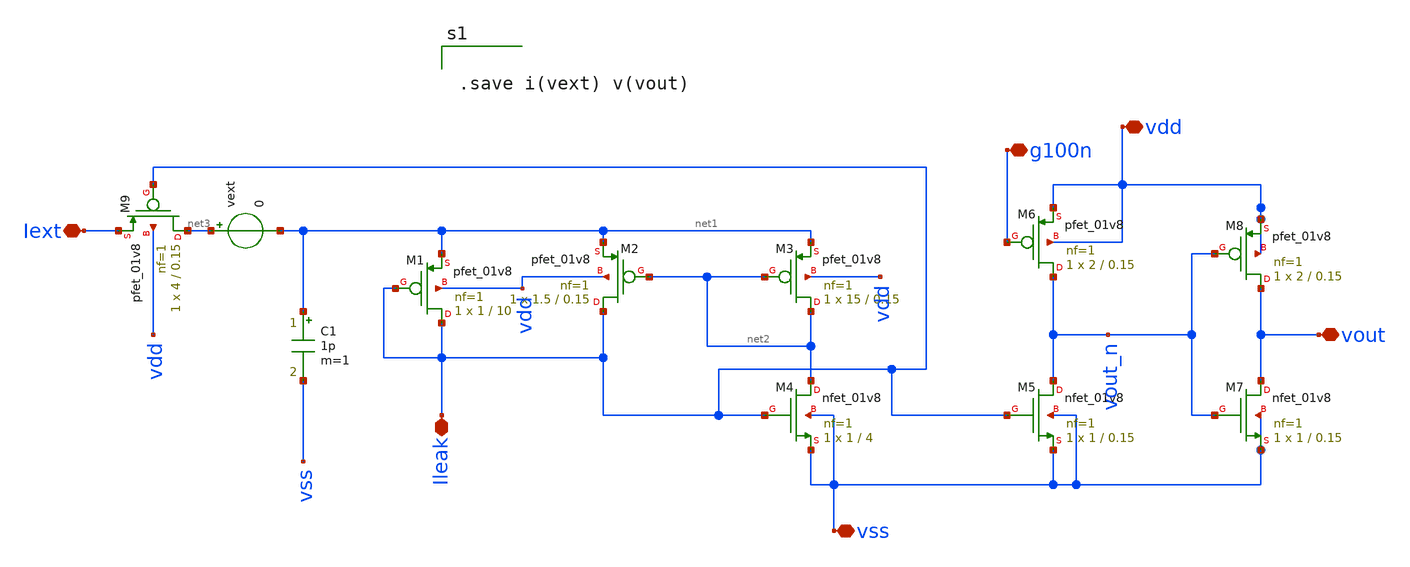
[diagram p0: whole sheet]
** sch_path: Neuron/ultralif/ul_tun.sch
**.subckt ul_tun Iext vout vss Ileak vdd g100n
*.iopin Iext
*.iopin vout
*.iopin vss
*.iopin Ileak
*.iopin vdd
*.iopin g100n
XM1 Ileak Ileak net1 vdd sky130_fd_pr__pfet_01v8 L=10 W=1 nf=1 ad='int((nf+1)/2) * W/nf * 0.29' as='int((nf+2)/2) * W/nf * 0.29'
+ pd='2*int((nf+1)/2) * (W/nf + 0.29)' ps='2*int((nf+2)/2) * (W/nf + 0.29)' nrd='0.29 / W' nrs='0.29 / W'
+ sa=0 sb=0 sd=0 mult=1 m=1
XM2 Ileak net2 net1 vdd sky130_fd_pr__pfet_01v8 L=0.15 W=1.5 nf=1 ad='int((nf+1)/2) * W/nf * 0.29' as='int((nf+2)/2) * W/nf * 0.29'
+ pd='2*int((nf+1)/2) * (W/nf + 0.29)' ps='2*int((nf+2)/2) * (W/nf + 0.29)' nrd='0.29 / W' nrs='0.29 / W'
+ sa=0 sb=0 sd=0 mult=1 m=1
XM3 net2 net2 net1 vdd sky130_fd_pr__pfet_01v8 L=0.15 W=15 nf=1 ad='int((nf+1)/2) * W/nf * 0.29' as='int((nf+2)/2) * W/nf * 0.29'
+ pd='2*int((nf+1)/2) * (W/nf + 0.29)' ps='2*int((nf+2)/2) * (W/nf + 0.29)' nrd='0.29 / W' nrs='0.29 / W'
+ sa=0 sb=0 sd=0 mult=1 m=1
XM4 net2 Ileak vss vss sky130_fd_pr__nfet_01v8 L=4 W=1 nf=1 ad='int((1 + 1)/2) * 1 / 1 * 0.29' as='int((1 + 2)/2) * 1 / 1 * 0.29'
+ pd='2*int((1 + 1)/2) * (1 / 1 + 0.29)' ps='2*int((1 + 2)/2) * (1 / 1 + 0.29)' nrd='0.29 / 1 ' nrs='0.29 / 1 '
+ sa=0 sb=0 sd=0 mult=1 m=1
C1 net1 vss 1p m=1
XM5 vout_n Ileak vss vss sky130_fd_pr__nfet_01v8 L=0.15 W=1 nf=1 ad='int((1 + 1)/2) * 1 / 1 * 0.29' as='int((1 + 2)/2) * 1 / 1 * 0.29'
+ pd='2*int((1 + 1)/2) * (1 / 1 + 0.29)' ps='2*int((1 + 2)/2) * (1 / 1 + 0.29)' nrd='0.29 / 1 ' nrs='0.29 / 1 '
+ sa=0 sb=0 sd=0 mult=1 m=1
XM6 vout_n g100n vdd vdd sky130_fd_pr__pfet_01v8 L=0.15 W=2 nf=1 ad='int((nf+1)/2) * W/nf * 0.29' as='int((nf+2)/2) * W/nf * 0.29'
+ pd='2*int((nf+1)/2) * (W/nf + 0.29)' ps='2*int((nf+2)/2) * (W/nf + 0.29)' nrd='0.29 / W' nrs='0.29 / W'
+ sa=0 sb=0 sd=0 mult=1 m=1
XM7 vout vout_n vss vss sky130_fd_pr__nfet_01v8 L=0.15 W=1 nf=1 ad='int((1 + 1)/2) * 1 / 1 * 0.29' as='int((1 + 2)/2) * 1 / 1 * 0.29'
+ pd='2*int((1 + 1)/2) * (1 / 1 + 0.29)' ps='2*int((1 + 2)/2) * (1 / 1 + 0.29)' nrd='0.29 / 1 ' nrs='0.29 / 1 '
+ sa=0 sb=0 sd=0 mult=1 m=1
XM8 vout vout_n vdd vdd sky130_fd_pr__pfet_01v8 L=0.15 W=2 nf=1 ad='int((nf+1)/2) * W/nf * 0.29' as='int((nf+2)/2) * W/nf * 0.29'
+ pd='2*int((nf+1)/2) * (W/nf + 0.29)' ps='2*int((nf+2)/2) * (W/nf + 0.29)' nrd='0.29 / W' nrs='0.29 / W'
+ sa=0 sb=0 sd=0 mult=1 m=1
XM9 net3 Ileak Iext vdd sky130_fd_pr__pfet_01v8 L=0.15 W=4 nf=1 ad='int((nf+1)/2) * W/nf * 0.29' as='int((nf+2)/2) * W/nf * 0.29'
+ pd='2*int((nf+1)/2) * (W/nf + 0.29)' ps='2*int((nf+2)/2) * (W/nf + 0.29)' nrd='0.29 / W' nrs='0.29 / W'
+ sa=0 sb=0 sd=0 mult=1 m=1
vext net3 net1 0
**** begin user architecture code


.save i(vext) v(vout)


**** end user architecture code
**.ends
.end
